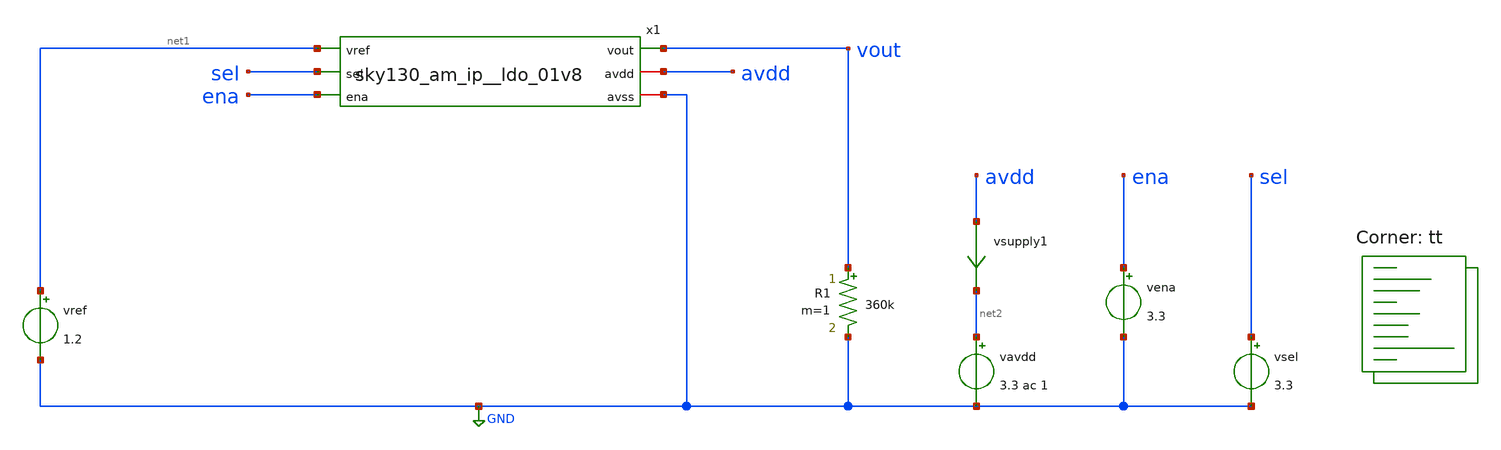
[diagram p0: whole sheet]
** sch_path: xschem/sky130_am_ip__ldo_01v8_tb.sch
**.subckt sky130_am_ip__ldo_01v8_tb
x1 vout net1 sel ena avdd GND sky130_am_ip__ldo_01v8
R1 vout GND 360k m=1
vavdd net2 GND 3.3 ac 1
vsupply1 avdd net2 0
.save i(vsupply1)
vena ena GND 3.3
vref net1 GND 1.2
vsel sel GND 3.3
**** begin user architecture code

.option savecurrents
.control
save all

op
write sky130_am_ip__ldo_01v8_tb.raw
set appendwrite

ac dec 10 10 1e9
set units=degrees
plot db(vout)
*
* dc vavdd 0 3.3 100m
* plot vout
.endc


.lib $::SKYWATER_MODELS/sky130.lib.spice tt
**** end user architecture code
**.ends
.GLOBAL GND
.end
